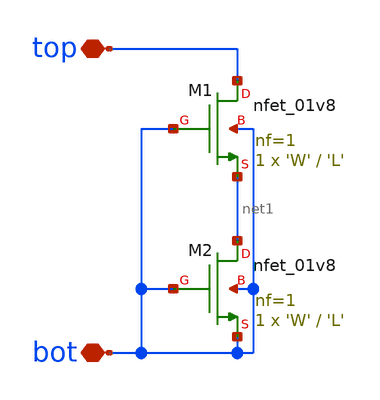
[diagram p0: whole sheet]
** sch_path: xschem/dschr_nwks/dschr_nwk_2t_type_b.sch
**.subckt dschr_nwk_2t_type_b top bot
*.iopin top
*.iopin bot
XM1 top bot net1 bot sky130_fd_pr__nfet_01v8 L='L' W='W' nf=1 ad='int((nf+1)/2) * W/nf * 0.29' as='int((nf+2)/2) * W/nf * 0.29'
+ pd='2*int((nf+1)/2) * (W/nf + 0.29)' ps='2*int((nf+2)/2) * (W/nf + 0.29)' nrd='0.29 / W' nrs='0.29 / W'
+ sa=0 sb=0 sd=0 mult=1 m=1
XM2 net1 bot bot bot sky130_fd_pr__nfet_01v8 L='L' W='W' nf=1 ad='int((nf+1)/2) * W/nf * 0.29' as='int((nf+2)/2) * W/nf * 0.29'
+ pd='2*int((nf+1)/2) * (W/nf + 0.29)' ps='2*int((nf+2)/2) * (W/nf + 0.29)' nrd='0.29 / W' nrs='0.29 / W'
+ sa=0 sb=0 sd=0 mult=1 m=1
**.ends
.end
